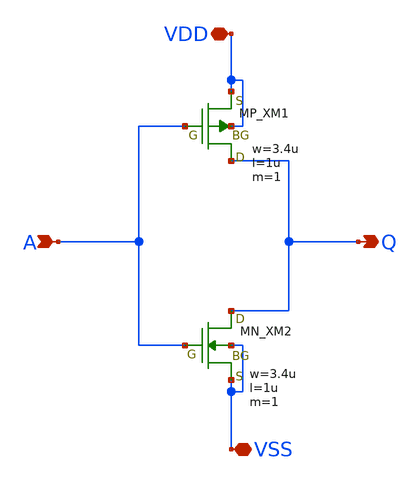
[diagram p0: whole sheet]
** sch_path: schematic/20250924_OSS_Workshop/Qdai/inverter_MUX_02/inv_shotaro_mori.sch
**.subckt inv_shotaro_mori VSS VDD A Q
*.iopin VSS
*.iopin VDD
*.ipin A
*.opin Q
XM1 Q A VDD VDD PMOS w=3.4u l=1u as=0 ad=0 ps=0 pd=0 nrd=0 nrs=0 m=1
XM2 Q A VSS VSS NMOS w=3.4u l=1u as=0 ad=0 ps=0 pd=0 nrd=0 nrs=0 m=1
**.ends
.end
